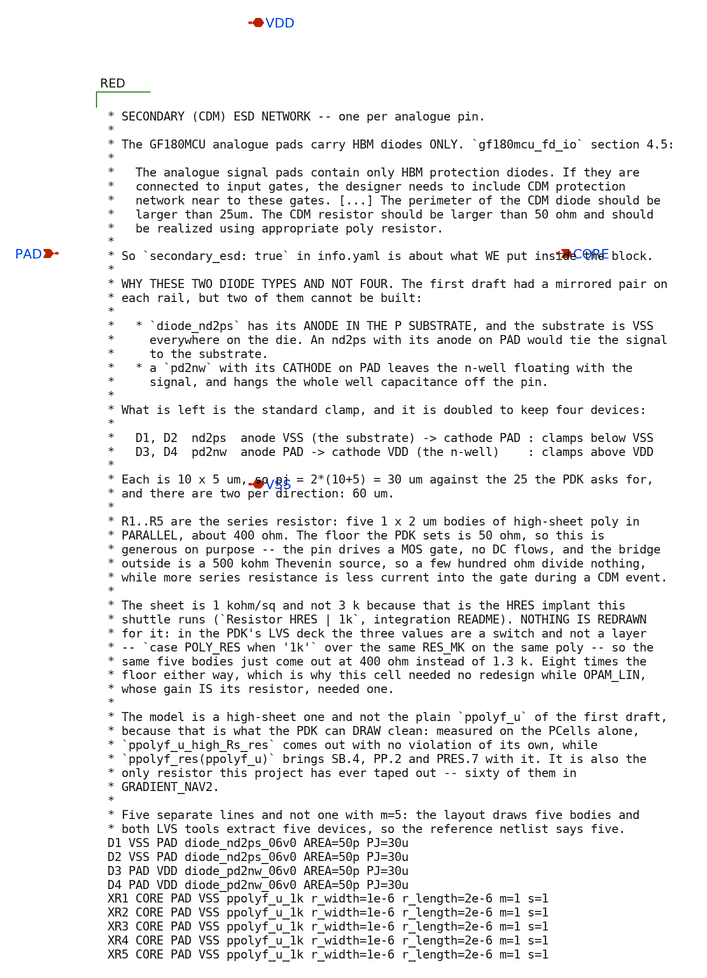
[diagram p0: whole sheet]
** sch_path: FINAL/XSCHEM_v2/ESD_CDM.sch
**.subckt ESD_CDM PAD CORE VDD VSS
*.ipin PAD
*.opin CORE
*.iopin VDD
*.iopin VSS
**** begin user architecture code


* SECONDARY (CDM) ESD NETWORK -- one per analogue pin.
*
* The GF180MCU analogue pads carry HBM diodes ONLY. `gf180mcu_fd_io` section 4.5:
*
*   The analogue signal pads contain only HBM protection diodes. If they are
*   connected to input gates, the designer needs to include CDM protection
*   network near to these gates. [...] The perimeter of the CDM diode should be
*   larger than 25um. The CDM resistor should be larger than 50 ohm and should
*   be realized using appropriate poly resistor.
*
* So `secondary_esd: true` in info.yaml is about what WE put inside the block.
*
* WHY THESE TWO DIODE TYPES AND NOT FOUR. The first draft had a mirrored pair on
* each rail, but two of them cannot be built:
*
*   * `diode_nd2ps` has its ANODE IN THE P SUBSTRATE, and the substrate is VSS
*     everywhere on the die. An nd2ps with its anode on PAD would tie the signal
*     to the substrate.
*   * a `pd2nw` with its CATHODE on PAD leaves the n-well floating with the
*     signal, and hangs the whole well capacitance off the pin.
*
* What is left is the standard clamp, and it is doubled to keep four devices:
*
*   D1, D2  nd2ps  anode VSS (the substrate) -> cathode PAD : clamps below VSS
*   D3, D4  pd2nw  anode PAD -> cathode VDD (the n-well)    : clamps above VDD
*
* Each is 10 x 5 um, so pj = 2*(10+5) = 30 um against the 25 the PDK asks for,
* and there are two per direction: 60 um.
*
* R1..R5 are the series resistor: five 1 x 2 um bodies of high-sheet poly in
* PARALLEL, about 400 ohm. The floor the PDK sets is 50 ohm, so this is
* generous on purpose -- the pin drives a MOS gate, no DC flows, and the bridge
* outside is a 500 kohm Thevenin source, so a few hundred ohm divide nothing,
* while more series resistance is less current into the gate during a CDM event.
*
* The sheet is 1 kohm/sq and not 3 k because that is the HRES implant this
* shuttle runs (`Resistor HRES | 1k`, integration README). NOTHING IS REDRAWN
* for it: in the PDK's LVS deck the three values are a switch and not a layer
* -- `case POLY_RES when '1k'` over the same RES_MK on the same poly -- so the
* same five bodies just come out at 400 ohm instead of 1.3 k. Eight times the
* floor either way, which is why this cell needed no redesign while OPAM_LIN,
* whose gain IS its resistor, needed one.
*
* The model is a high-sheet one and not the plain `ppolyf_u` of the first draft,
* because that is what the PDK can DRAW clean: measured on the PCells alone,
* `ppolyf_u_high_Rs_res` comes out with no violation of its own, while
* `ppolyf_res(ppolyf_u)` brings SB.4, PP.2 and PRES.7 with it. It is also the
* only resistor this project has ever taped out -- sixty of them in
* GRADIENT_NAV2.
*
* Five separate lines and not one with m=5: the layout draws five bodies and
* both LVS tools extract five devices, so the reference netlist says five.
D1 VSS PAD diode_nd2ps_06v0 AREA=50p PJ=30u
D2 VSS PAD diode_nd2ps_06v0 AREA=50p PJ=30u
D3 PAD VDD diode_pd2nw_06v0 AREA=50p PJ=30u
D4 PAD VDD diode_pd2nw_06v0 AREA=50p PJ=30u
XR1 CORE PAD VSS ppolyf_u_1k r_width=1e-6 r_length=2e-6 m=1 s=1
XR2 CORE PAD VSS ppolyf_u_1k r_width=1e-6 r_length=2e-6 m=1 s=1
XR3 CORE PAD VSS ppolyf_u_1k r_width=1e-6 r_length=2e-6 m=1 s=1
XR4 CORE PAD VSS ppolyf_u_1k r_width=1e-6 r_length=2e-6 m=1 s=1
XR5 CORE PAD VSS ppolyf_u_1k r_width=1e-6 r_length=2e-6 m=1 s=1


**** end user architecture code
**.ends
.end
